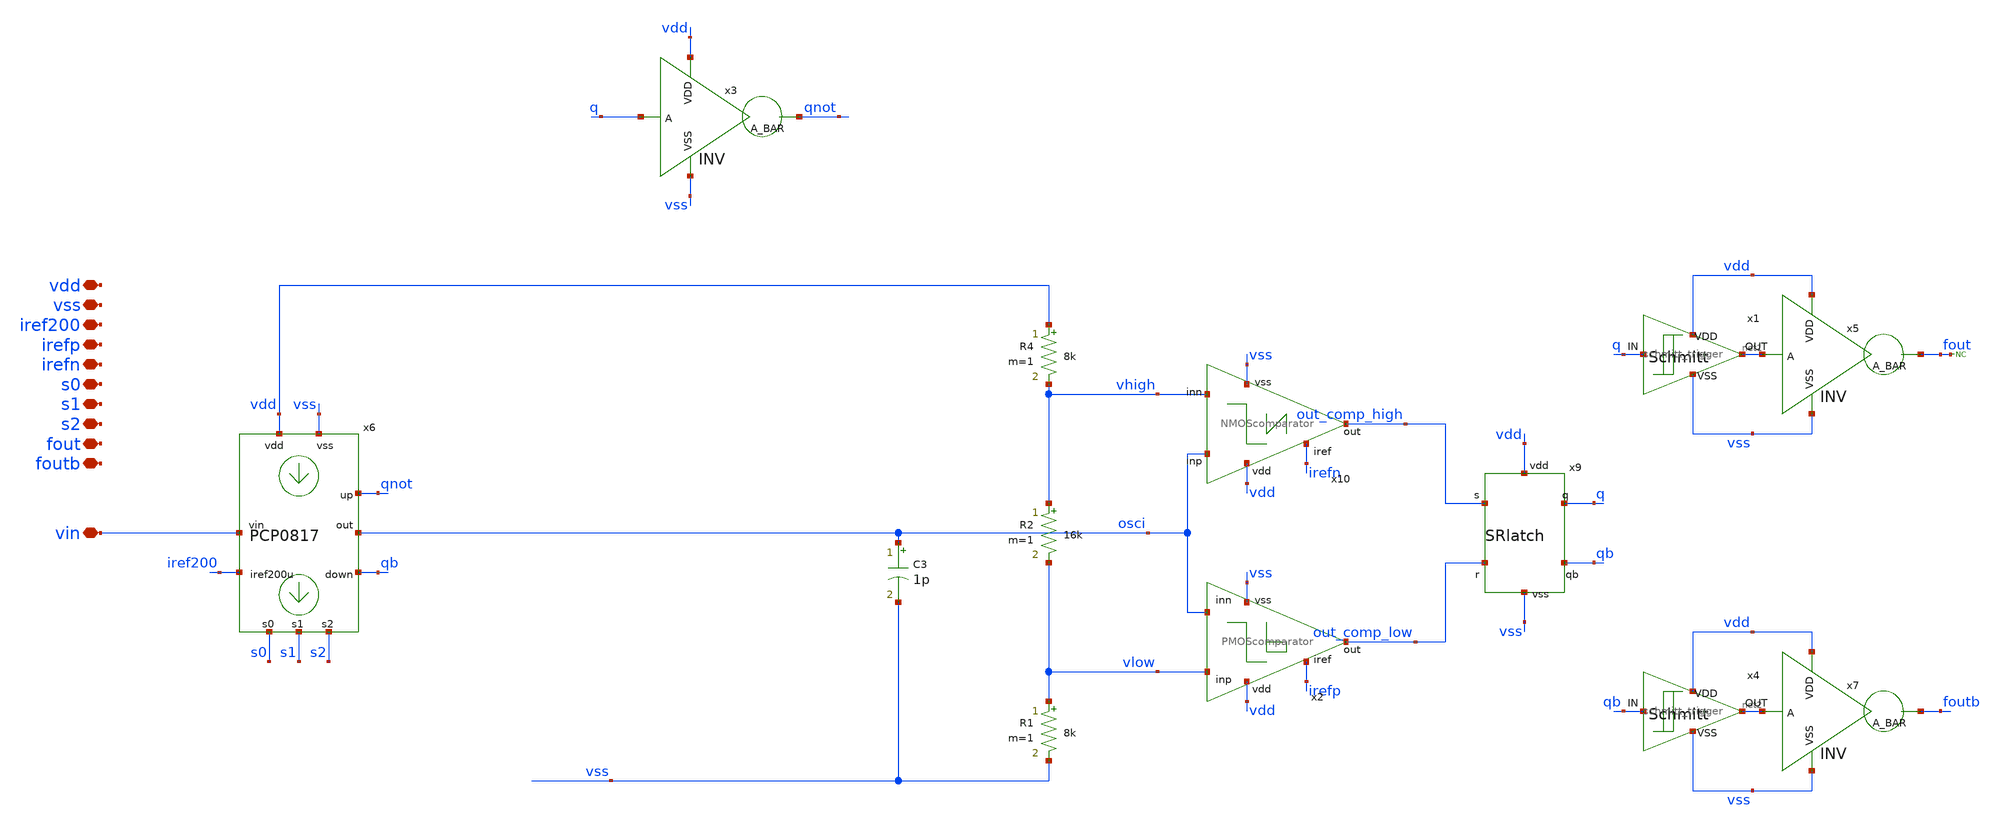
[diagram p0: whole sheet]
** sch_path: designs/libs/qw_core_analog/VCO0831_noTG/VCO0831_noTG.sch
**.subckt VCO0831_noTG vin vdd vss iref200 irefp irefn s0 s1 s2 fout foutb
*.iopin vin
*.iopin vdd
*.iopin vss
*.iopin iref200
*.iopin irefp
*.iopin irefn
*.iopin s0
*.iopin s1
*.iopin s2
*.iopin fout
*.iopin foutb
R1 vlow vss 8k m=1
R2 vhigh vlow 16k m=1
R4 vdd vhigh 8k m=1
x9 vdd out_comp_high q qb out_comp_low vss SRlatch
x2 vdd irefp vlow out_comp_low osci vss PMOScomparator
x10 vdd osci out_comp_high vhigh irefn vss NMOScomparator
x3 vdd q qnot vss INV
x1 q net1 vdd vss schmitt_trigger
x4 qb net2 vdd vss schmitt_trigger
x5 vdd net1 fout vss INV
x7 vdd net2 foutb vss INV
* noconn fout
C3 osci vss 1p m=1
x6 vdd vss vin iref200 osci qnot qb s0 s1 s2 PCP0817
**.ends
.end
